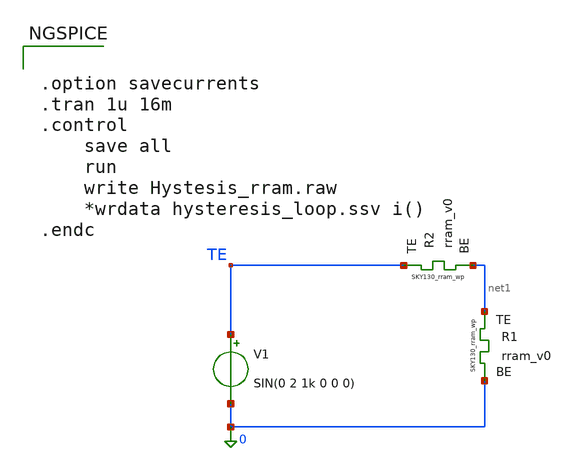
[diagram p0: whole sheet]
** sch_path: Ricardo/STDP_test/hysteresis_rram.sch
**.subckt hysteresis_rram
XR1 net1 0 rram_v0
V1 TE 0 SIN(0 2 1k 0 0 0)
XR2 TE net1 rram_v0
**** begin user architecture code

** opencircuitdesign pdks install
.inc $::SKYWATER_MODELS/rram_v0.spice



.option savecurrents
.tran 1u 16m
.control
	save all
	run
	write Hystesis_rram.raw
	*wrdata hysteresis_loop.ssv i()
.endc



**** end user architecture code
**.ends
.end
